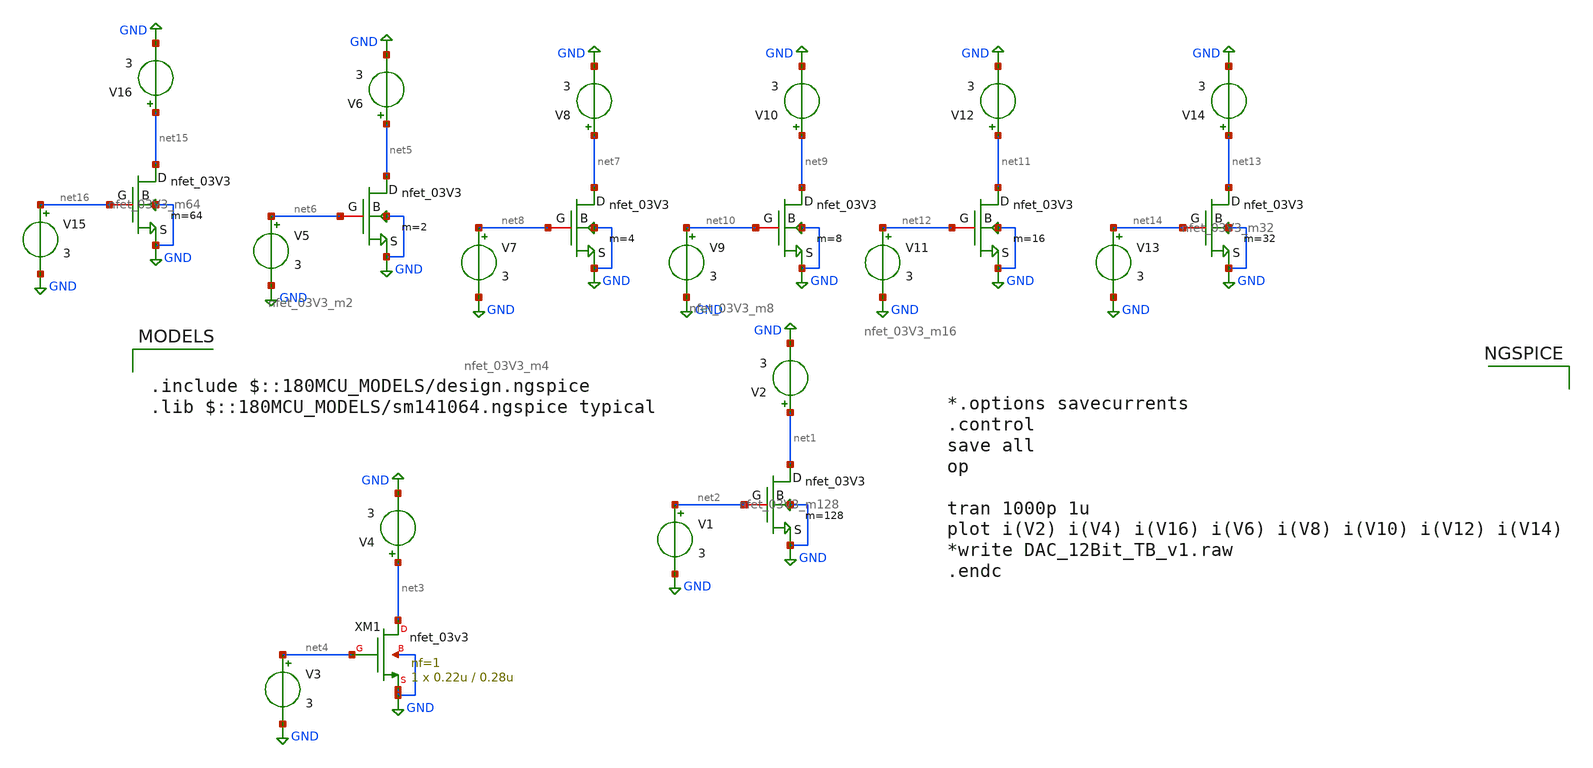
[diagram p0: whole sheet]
** sch_path: DAC_PAKISTAN_01/Pakistan1_Xschem/m8tb.sch
**.subckt m8tb
V1 net2 GND 3
V2 net1 GND 3
V3 net4 GND 3
V4 net3 GND 3
XM1 net3 net4 GND GND nfet_03v3 L=0.28u W=0.22u nf=1 ad='int((nf+1)/2) * W/nf * 0.18u' as='int((nf+2)/2) * W/nf * 0.18u'
+ pd='2*int((nf+1)/2) * (W/nf + 0.18u)' ps='2*int((nf+2)/2) * (W/nf + 0.18u)' nrd='0.18u / W' nrs='0.18u / W'
+ sa=0 sb=0 sd=0 m=1
x1 GND net1 GND net2 nfet_03V3_m128
V5 net6 GND 3
V6 net5 GND 3
V7 net8 GND 3
V8 net7 GND 3
V9 net10 GND 3
V10 net9 GND 3
V11 net12 GND 3
V12 net11 GND 3
V13 net14 GND 3
V14 net13 GND 3
x2 GND net5 GND net6 nfet_03V3_m2
x3 GND net7 GND net8 nfet_03V3_m4
x4 GND net9 GND net10 nfet_03V3_m8
x5 GND net11 GND net12 nfet_03V3_m16
x6 GND net13 GND net14 nfet_03V3_m32
x7 GND net15 GND net16 nfet_03V3_m64
V15 net16 GND 3
V16 net15 GND 3
**** begin user architecture code

.include $::180MCU_MODELS/design.ngspice
.lib $::180MCU_MODELS/sm141064.ngspice typical



*.options savecurrents
.control
save all
op

tran 1000p 1u
plot i(V2) i(V4) i(V16) i(V6) i(V8) i(V10) i(V12) i(V14)
*write DAC_12Bit_TB_v1.raw
.endc


**** end user architecture code
**.ends
.GLOBAL GND
.end
